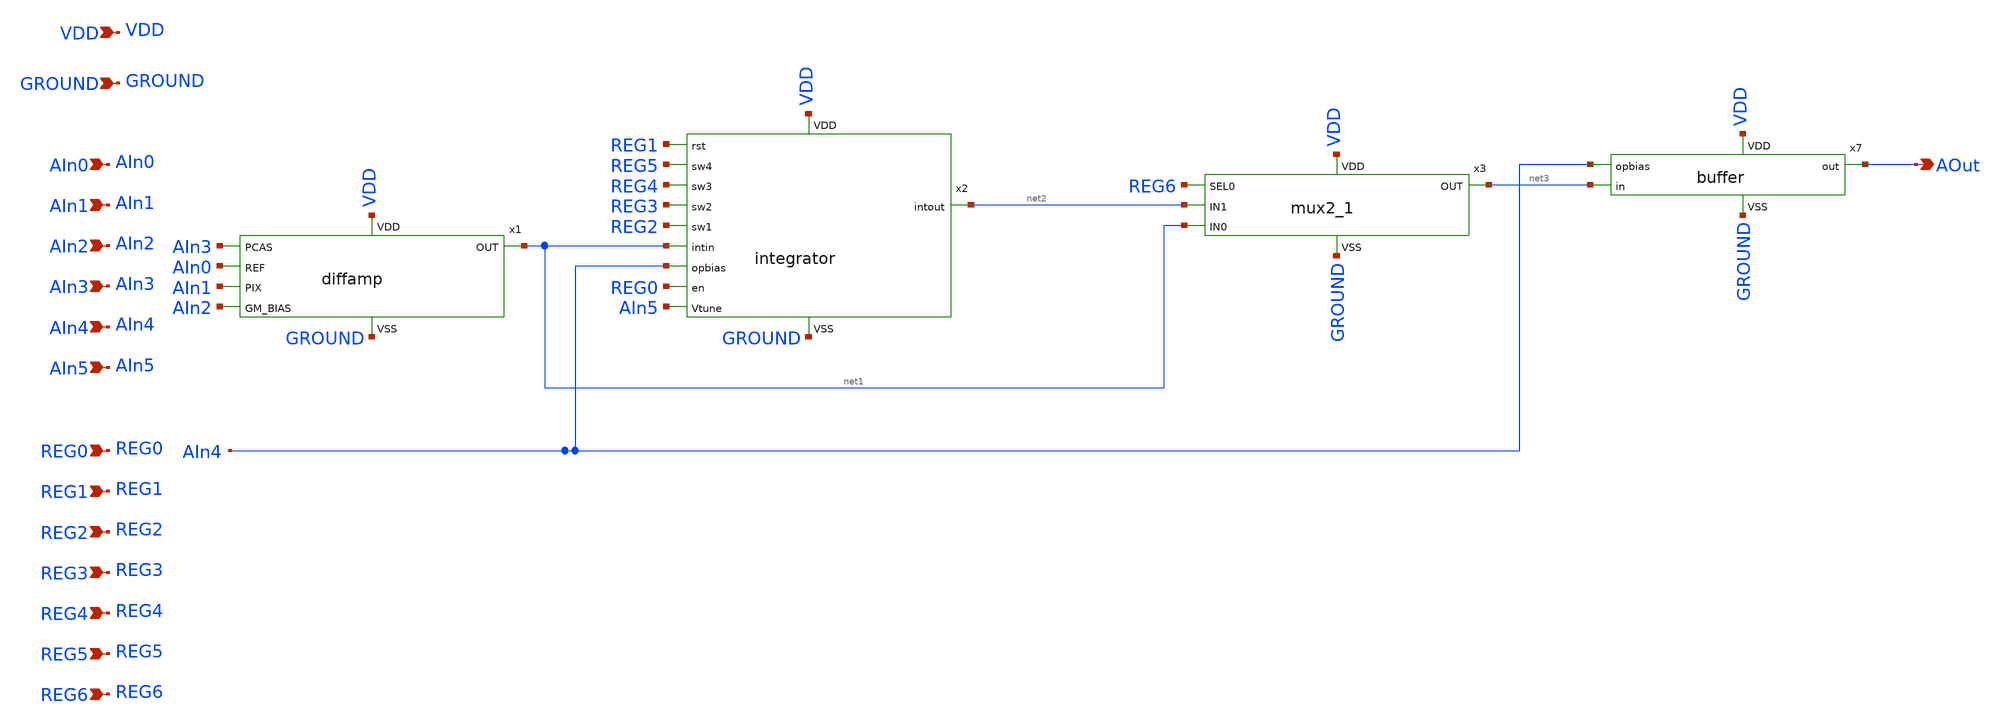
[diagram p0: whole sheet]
** sch_path: xschem/ColROs.sch
**.subckt ColROs AOut REG1 REG2 REG3 REG0 REG5 REG6 REG4 AIn0 AIn1 AIn2 AIn3 AIn4 AIn5 GROUND VDD
*.opin AOut
*.ipin REG1
*.ipin REG2
*.ipin REG3
*.ipin REG0
*.ipin REG5
*.ipin REG6
*.ipin REG4
*.ipin AIn0
*.ipin AIn1
*.ipin AIn2
*.ipin AIn3
*.ipin AIn4
*.ipin AIn5
*.ipin GROUND
*.ipin VDD
x1 AIn3 net1 AIn0 AIn1 AIn2 VDD GROUND diffamp
x2 REG3 REG2 net1 net2 AIn4 REG0 AIn5 REG1 REG5 REG4 VDD GROUND integrator
x7 AIn4 net3 AOut GROUND VDD buffer
x3 REG6 net2 net3 net1 VDD GROUND mux2_1
**.ends
.end
